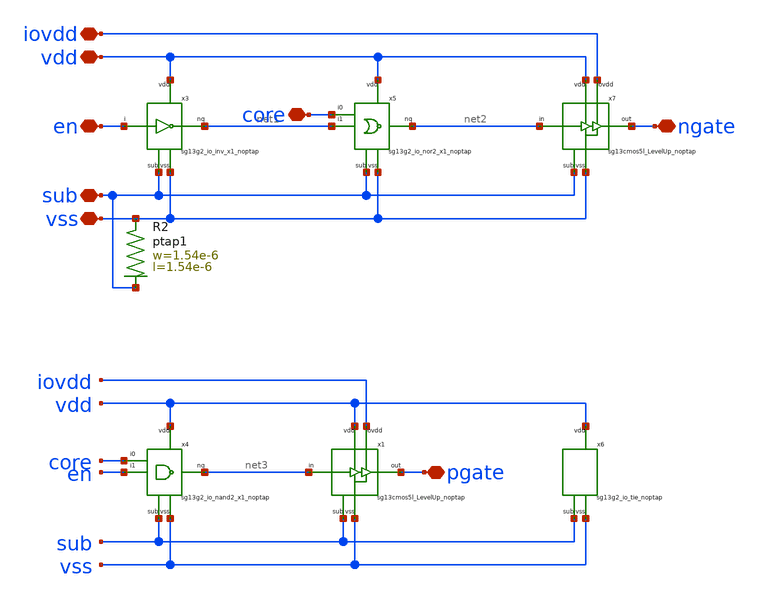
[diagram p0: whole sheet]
** sch_path: ihp-sg13cmos5l/libs.tech/xschem/hm_stdcells/sg13cmos5l_GateDecode.sch
**.subckt sg13cmos5l_GateDecode pgate ngate iovdd vss en vdd sub core
*.iopin pgate
*.iopin ngate
*.iopin iovdd
*.iopin vss
*.iopin en
*.iopin vdd
*.iopin sub
*.iopin core
x3 vss en net1 vdd sub sg13g2_io_inv_x1_noptap
x4 vss core net3 vdd sub en sg13g2_io_nand2_x1_noptap
x5 vss core net2 vdd sub net1 sg13g2_io_nor2_x1_noptap
x6 vss vdd sub sg13g2_io_tie_noptap
XR2 vss sub ptap1 R=114.9 w=1.54e-6 l=1.54e-6
x7 iovdd vss net2 ngate vdd sub sg13cmos5l_LevelUp_noptap
x1 iovdd vss net3 pgate vdd sub sg13cmos5l_LevelUp_noptap
**.ends
.end
